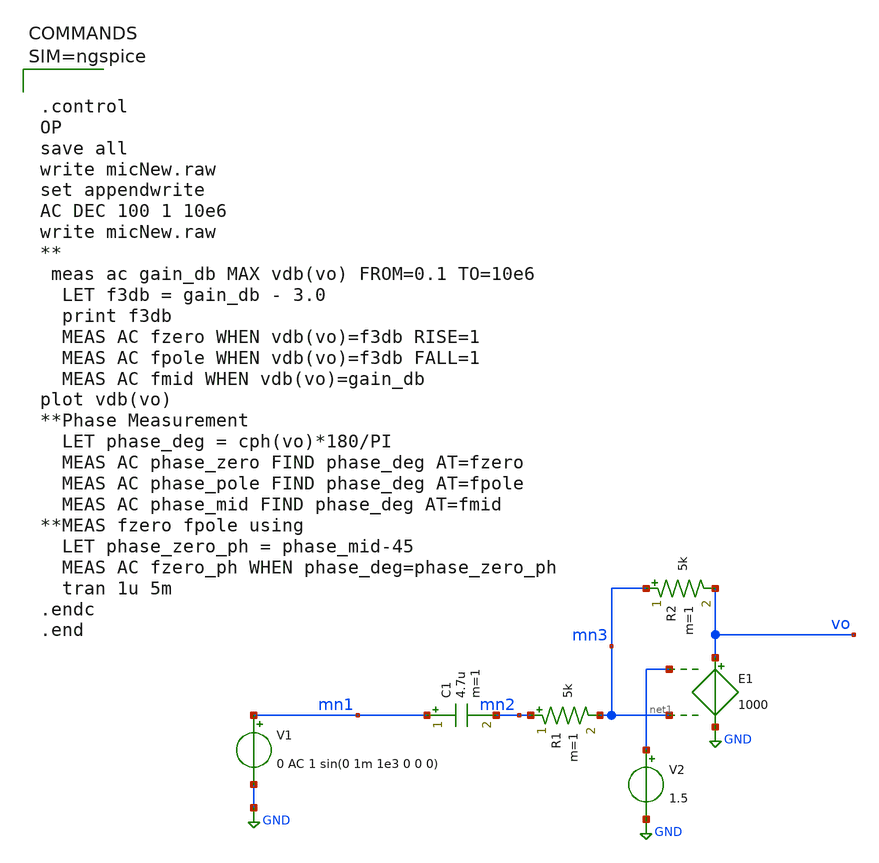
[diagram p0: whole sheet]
** sch_path: xschem/micNew.sch
**.subckt micNew
V1 mn1 GND 0 AC 1 sin(0 1m 1e3 0 0 0)
C1 mn1 mn2 4.7u m=1
R1 mn2 mn3 5k m=1
E1 vo GND net1 mn3 1000
R2 mn3 vo 5k m=1
V2 net1 GND 1.5
**** begin user architecture code



.control
OP
save all
write micNew.raw
set appendwrite
AC DEC 100 1 10e6
write micNew.raw
**
 meas ac gain_db MAX vdb(vo) FROM=0.1 TO=10e6
  LET f3db = gain_db - 3.0
  print f3db
  MEAS AC fzero WHEN vdb(vo)=f3db RISE=1
  MEAS AC fpole WHEN vdb(vo)=f3db FALL=1
  MEAS AC fmid WHEN vdb(vo)=gain_db
plot vdb(vo)
**Phase Measurement
  LET phase_deg = cph(vo)*180/PI
  MEAS AC phase_zero FIND phase_deg AT=fzero
  MEAS AC phase_pole FIND phase_deg AT=fpole
  MEAS AC phase_mid FIND phase_deg AT=fmid
**MEAS fzero fpole using
  LET phase_zero_ph = phase_mid-45
  MEAS AC fzero_ph WHEN phase_deg=phase_zero_ph
  tran 1u 5m
.endc
.end



**** end user architecture code
**.ends
.GLOBAL GND
.end
